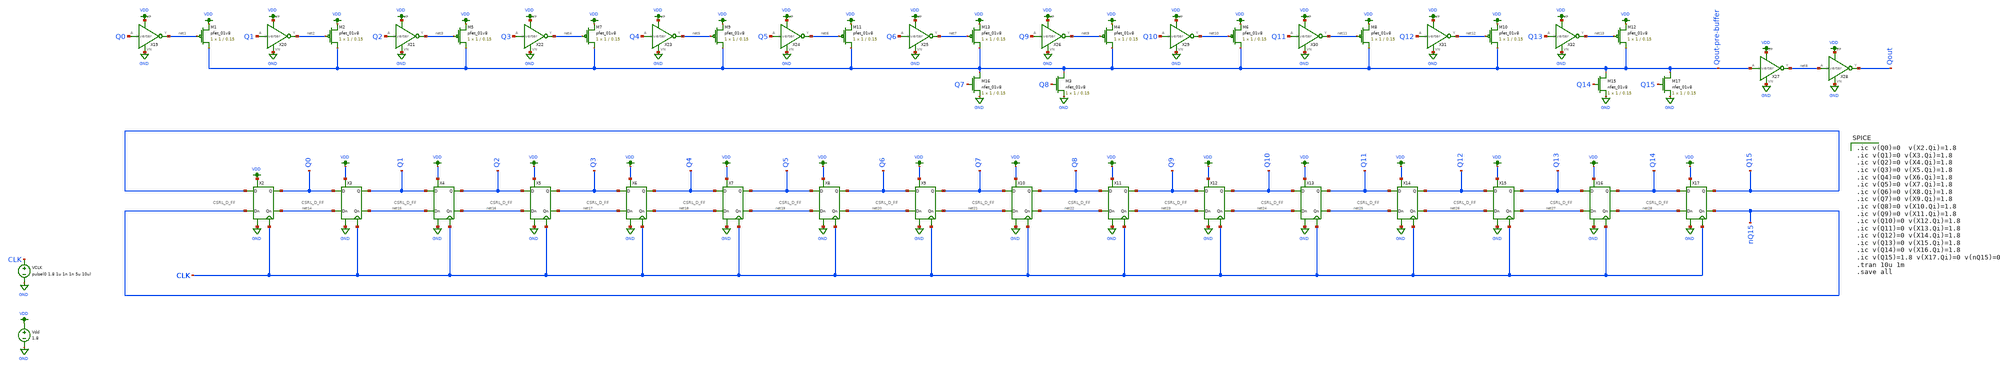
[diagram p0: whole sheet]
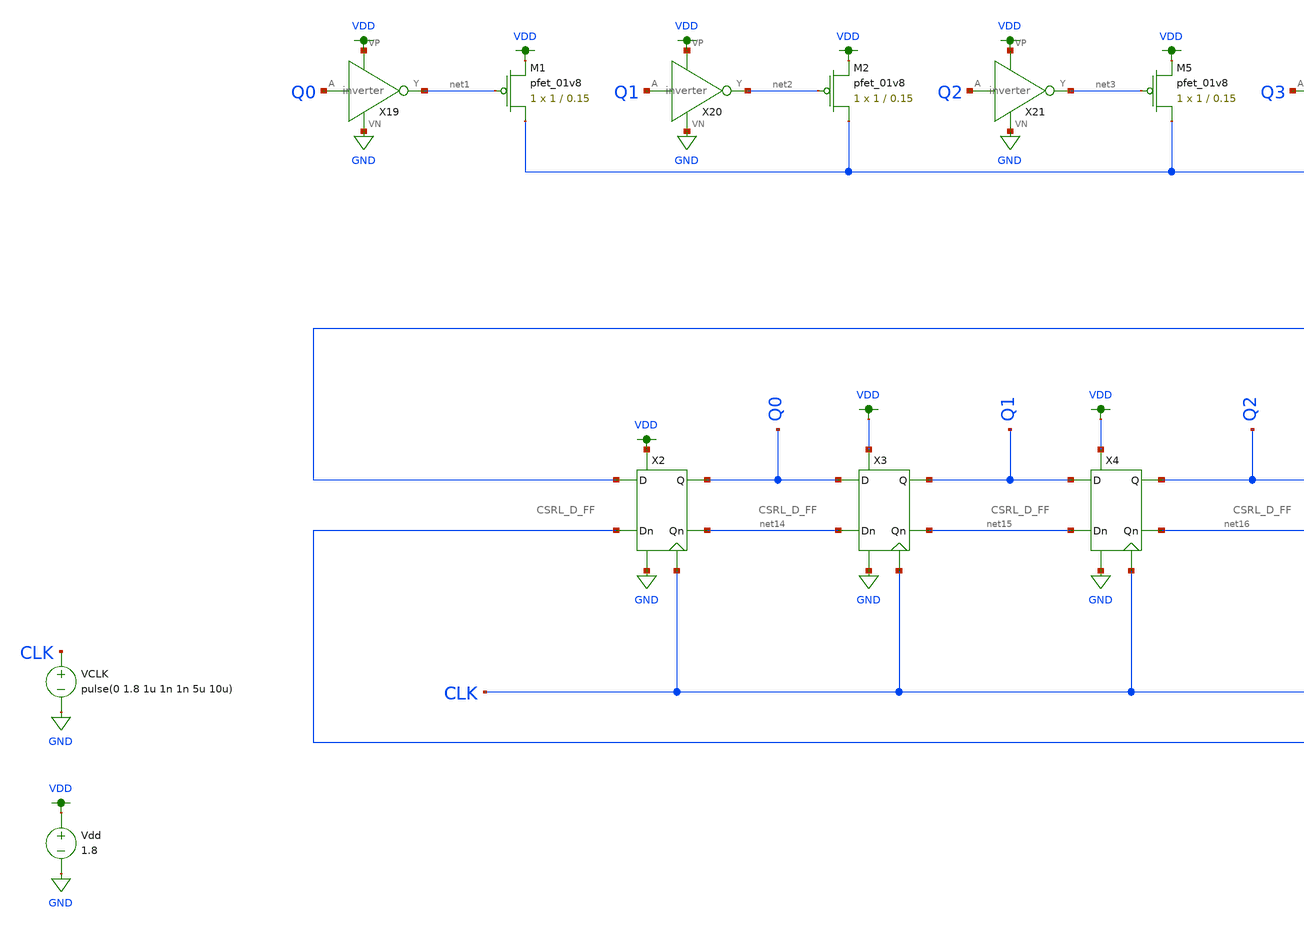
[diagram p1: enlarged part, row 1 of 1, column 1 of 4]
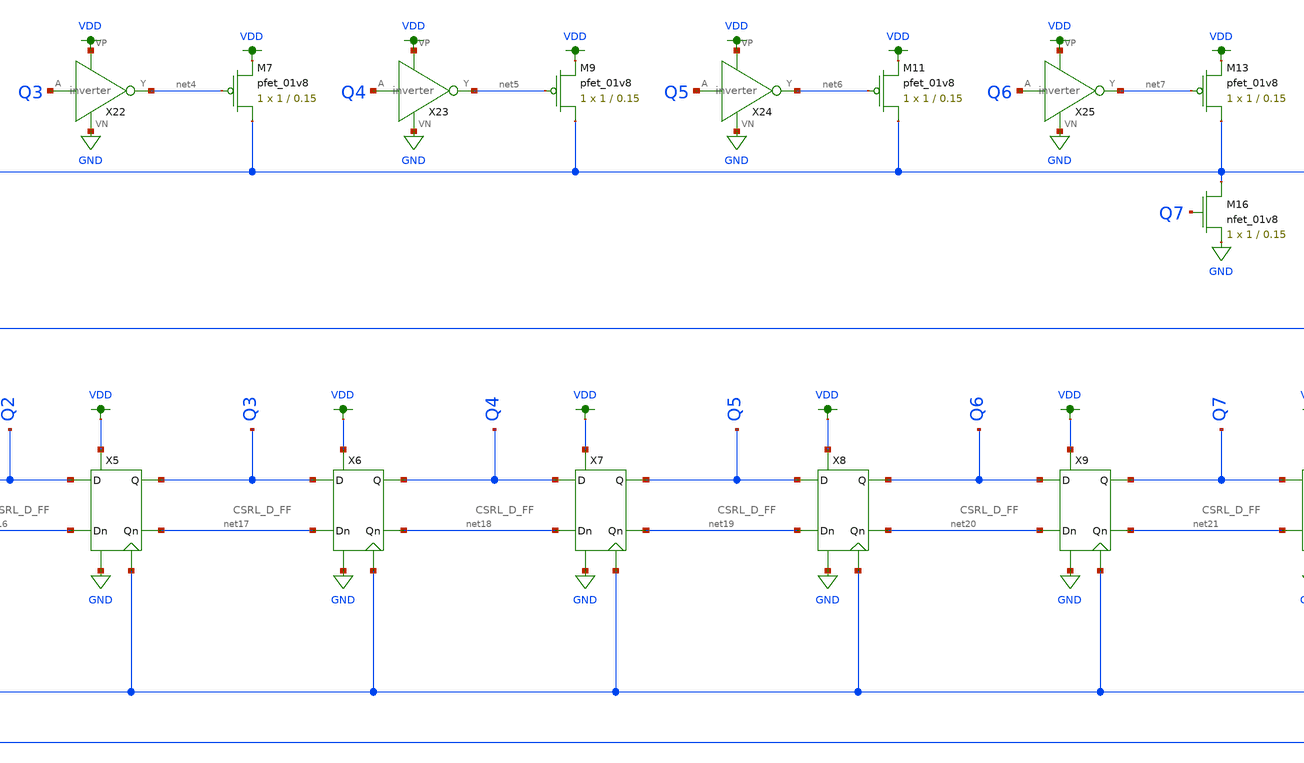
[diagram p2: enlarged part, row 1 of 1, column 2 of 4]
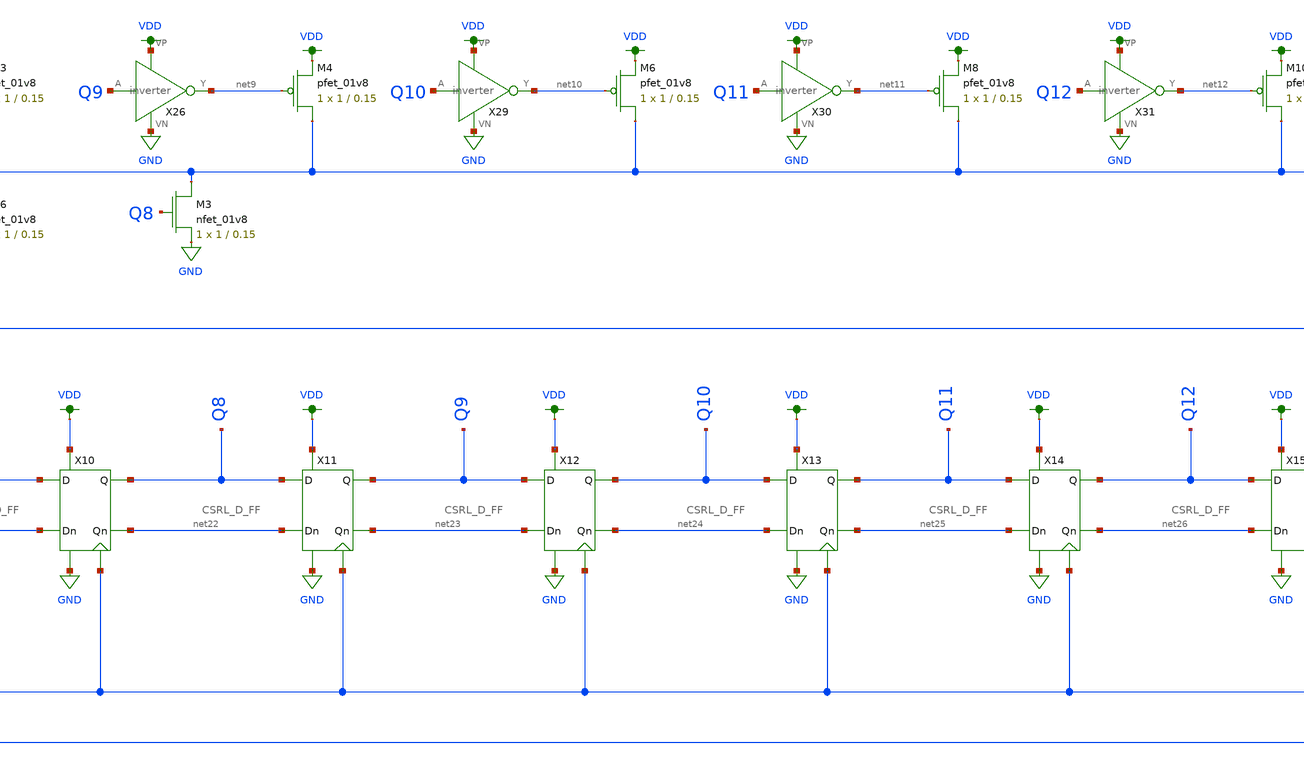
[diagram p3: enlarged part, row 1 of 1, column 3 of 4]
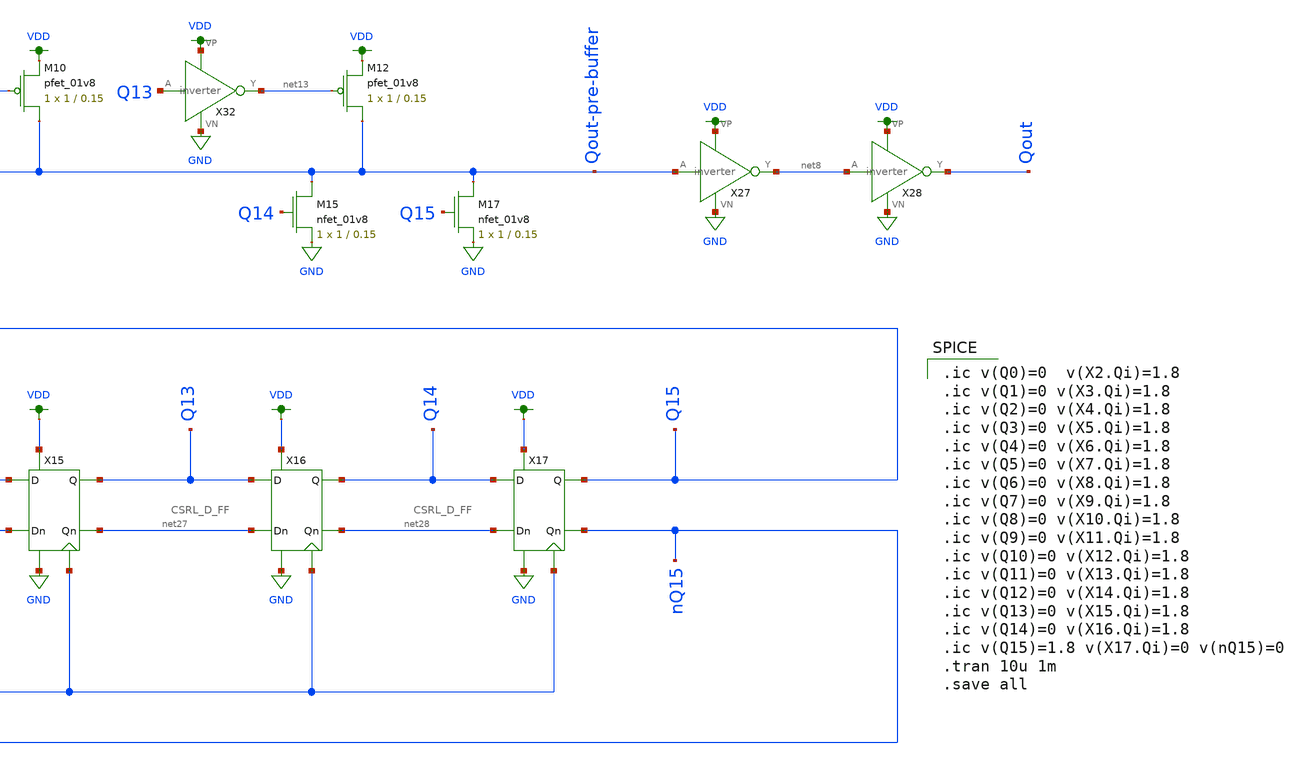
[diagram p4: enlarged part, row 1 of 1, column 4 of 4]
** sch_path: schematic/archive/phiF1.sch
**.subckt phiF1
VCLK CLK GND pulse(0 1.8 1u 1n 1n 5u 10u)
Vdd VDD GND 1.8
XM1 Qout-pre-buffer net1 VDD VDD sky130_fd_pr__pfet_01v8 L=0.15 W=1 nf=1 ad='int((nf+1)/2) * W/nf * 0.29'
+ as='int((nf+2)/2) * W/nf * 0.29' pd='2*int((nf+1)/2) * (W/nf + 0.29)' ps='2*int((nf+2)/2) * (W/nf + 0.29)'
+ nrd='0.29 / W' nrs='0.29 / W' sa=0 sb=0 sd=0 mult=1 m=1
XM2 Qout-pre-buffer net2 VDD VDD sky130_fd_pr__pfet_01v8 L=0.15 W=1 nf=1 ad='int((nf+1)/2) * W/nf * 0.29'
+ as='int((nf+2)/2) * W/nf * 0.29' pd='2*int((nf+1)/2) * (W/nf + 0.29)' ps='2*int((nf+2)/2) * (W/nf + 0.29)'
+ nrd='0.29 / W' nrs='0.29 / W' sa=0 sb=0 sd=0 mult=1 m=1
X19 Q0 net1 VDD GND inverter
X20 Q1 net2 VDD GND inverter
XM5 Qout-pre-buffer net3 VDD VDD sky130_fd_pr__pfet_01v8 L=0.15 W=1 nf=1 ad='int((nf+1)/2) * W/nf * 0.29'
+ as='int((nf+2)/2) * W/nf * 0.29' pd='2*int((nf+1)/2) * (W/nf + 0.29)' ps='2*int((nf+2)/2) * (W/nf + 0.29)'
+ nrd='0.29 / W' nrs='0.29 / W' sa=0 sb=0 sd=0 mult=1 m=1
X21 Q2 net3 VDD GND inverter
XM7 Qout-pre-buffer net4 VDD VDD sky130_fd_pr__pfet_01v8 L=0.15 W=1 nf=1 ad='int((nf+1)/2) * W/nf * 0.29'
+ as='int((nf+2)/2) * W/nf * 0.29' pd='2*int((nf+1)/2) * (W/nf + 0.29)' ps='2*int((nf+2)/2) * (W/nf + 0.29)'
+ nrd='0.29 / W' nrs='0.29 / W' sa=0 sb=0 sd=0 mult=1 m=1
X22 Q3 net4 VDD GND inverter
XM9 Qout-pre-buffer net5 VDD VDD sky130_fd_pr__pfet_01v8 L=0.15 W=1 nf=1 ad='int((nf+1)/2) * W/nf * 0.29'
+ as='int((nf+2)/2) * W/nf * 0.29' pd='2*int((nf+1)/2) * (W/nf + 0.29)' ps='2*int((nf+2)/2) * (W/nf + 0.29)'
+ nrd='0.29 / W' nrs='0.29 / W' sa=0 sb=0 sd=0 mult=1 m=1
X23 Q4 net5 VDD GND inverter
XM11 Qout-pre-buffer net6 VDD VDD sky130_fd_pr__pfet_01v8 L=0.15 W=1 nf=1 ad='int((nf+1)/2) * W/nf * 0.29'
+ as='int((nf+2)/2) * W/nf * 0.29' pd='2*int((nf+1)/2) * (W/nf + 0.29)' ps='2*int((nf+2)/2) * (W/nf + 0.29)'
+ nrd='0.29 / W' nrs='0.29 / W' sa=0 sb=0 sd=0 mult=1 m=1
X24 Q5 net6 VDD GND inverter
XM13 Qout-pre-buffer net7 VDD VDD sky130_fd_pr__pfet_01v8 L=0.15 W=1 nf=1 ad='int((nf+1)/2) * W/nf * 0.29'
+ as='int((nf+2)/2) * W/nf * 0.29' pd='2*int((nf+1)/2) * (W/nf + 0.29)' ps='2*int((nf+2)/2) * (W/nf + 0.29)'
+ nrd='0.29 / W' nrs='0.29 / W' sa=0 sb=0 sd=0 mult=1 m=1
X25 Q6 net7 VDD GND inverter
XM16 Qout-pre-buffer Q7 GND GND sky130_fd_pr__nfet_01v8 L=0.15 W=1 nf=1 ad='int((nf+1)/2) * W/nf * 0.29'
+ as='int((nf+2)/2) * W/nf * 0.29' pd='2*int((nf+1)/2) * (W/nf + 0.29)' ps='2*int((nf+2)/2) * (W/nf + 0.29)'
+ nrd='0.29 / W' nrs='0.29 / W' sa=0 sb=0 sd=0 mult=1 m=1
X27 Qout-pre-buffer net8 VDD GND inverter
X28 net8 Qout VDD GND inverter
XM3 Qout-pre-buffer Q8 GND GND sky130_fd_pr__nfet_01v8 L=0.15 W=1 nf=1 ad='int((nf+1)/2) * W/nf * 0.29'
+ as='int((nf+2)/2) * W/nf * 0.29' pd='2*int((nf+1)/2) * (W/nf + 0.29)' ps='2*int((nf+2)/2) * (W/nf + 0.29)'
+ nrd='0.29 / W' nrs='0.29 / W' sa=0 sb=0 sd=0 mult=1 m=1
XM4 Qout-pre-buffer net9 VDD VDD sky130_fd_pr__pfet_01v8 L=0.15 W=1 nf=1 ad='int((nf+1)/2) * W/nf * 0.29'
+ as='int((nf+2)/2) * W/nf * 0.29' pd='2*int((nf+1)/2) * (W/nf + 0.29)' ps='2*int((nf+2)/2) * (W/nf + 0.29)'
+ nrd='0.29 / W' nrs='0.29 / W' sa=0 sb=0 sd=0 mult=1 m=1
X26 Q9 net9 VDD GND inverter
XM6 Qout-pre-buffer net10 VDD VDD sky130_fd_pr__pfet_01v8 L=0.15 W=1 nf=1 ad='int((nf+1)/2) * W/nf * 0.29'
+ as='int((nf+2)/2) * W/nf * 0.29' pd='2*int((nf+1)/2) * (W/nf + 0.29)' ps='2*int((nf+2)/2) * (W/nf + 0.29)'
+ nrd='0.29 / W' nrs='0.29 / W' sa=0 sb=0 sd=0 mult=1 m=1
X29 Q10 net10 VDD GND inverter
XM8 Qout-pre-buffer net11 VDD VDD sky130_fd_pr__pfet_01v8 L=0.15 W=1 nf=1 ad='int((nf+1)/2) * W/nf * 0.29'
+ as='int((nf+2)/2) * W/nf * 0.29' pd='2*int((nf+1)/2) * (W/nf + 0.29)' ps='2*int((nf+2)/2) * (W/nf + 0.29)'
+ nrd='0.29 / W' nrs='0.29 / W' sa=0 sb=0 sd=0 mult=1 m=1
X30 Q11 net11 VDD GND inverter
XM10 Qout-pre-buffer net12 VDD VDD sky130_fd_pr__pfet_01v8 L=0.15 W=1 nf=1 ad='int((nf+1)/2) * W/nf * 0.29'
+ as='int((nf+2)/2) * W/nf * 0.29' pd='2*int((nf+1)/2) * (W/nf + 0.29)' ps='2*int((nf+2)/2) * (W/nf + 0.29)'
+ nrd='0.29 / W' nrs='0.29 / W' sa=0 sb=0 sd=0 mult=1 m=1
X31 Q12 net12 VDD GND inverter
XM12 Qout-pre-buffer net13 VDD VDD sky130_fd_pr__pfet_01v8 L=0.15 W=1 nf=1 ad='int((nf+1)/2) * W/nf * 0.29'
+ as='int((nf+2)/2) * W/nf * 0.29' pd='2*int((nf+1)/2) * (W/nf + 0.29)' ps='2*int((nf+2)/2) * (W/nf + 0.29)'
+ nrd='0.29 / W' nrs='0.29 / W' sa=0 sb=0 sd=0 mult=1 m=1
X32 Q13 net13 VDD GND inverter
XM15 Qout-pre-buffer Q14 GND GND sky130_fd_pr__nfet_01v8 L=0.15 W=1 nf=1 ad='int((nf+1)/2) * W/nf * 0.29'
+ as='int((nf+2)/2) * W/nf * 0.29' pd='2*int((nf+1)/2) * (W/nf + 0.29)' ps='2*int((nf+2)/2) * (W/nf + 0.29)'
+ nrd='0.29 / W' nrs='0.29 / W' sa=0 sb=0 sd=0 mult=1 m=1
XM17 Qout-pre-buffer Q15 GND GND sky130_fd_pr__nfet_01v8 L=0.15 W=1 nf=1 ad='int((nf+1)/2) * W/nf * 0.29'
+ as='int((nf+2)/2) * W/nf * 0.29' pd='2*int((nf+1)/2) * (W/nf + 0.29)' ps='2*int((nf+2)/2) * (W/nf + 0.29)'
+ nrd='0.29 / W' nrs='0.29 / W' sa=0 sb=0 sd=0 mult=1 m=1
X2 nQ15 Q15 net14 Q0 GND VDD CLK CSRL_D_FF
X3 net14 Q0 net15 Q1 GND VDD CLK CSRL_D_FF
X4 net15 Q1 net16 Q2 GND VDD CLK CSRL_D_FF
X5 net16 Q2 net17 Q3 GND VDD CLK CSRL_D_FF
X6 net17 Q3 net18 Q4 GND VDD CLK CSRL_D_FF
X7 net18 Q4 net19 Q5 GND VDD CLK CSRL_D_FF
X8 net19 Q5 net20 Q6 GND VDD CLK CSRL_D_FF
X9 net20 Q6 net21 Q7 GND VDD CLK CSRL_D_FF
X10 net21 Q7 net22 Q8 GND VDD CLK CSRL_D_FF
X11 net22 Q8 net23 Q9 GND VDD CLK CSRL_D_FF
X12 net23 Q9 net24 Q10 GND VDD CLK CSRL_D_FF
X13 net24 Q10 net25 Q11 GND VDD CLK CSRL_D_FF
X14 net25 Q11 net26 Q12 GND VDD CLK CSRL_D_FF
X15 net26 Q12 net27 Q13 GND VDD CLK CSRL_D_FF
X16 net27 Q13 net28 Q14 GND VDD CLK CSRL_D_FF
X17 net28 Q14 nQ15 Q15 GND VDD CLK CSRL_D_FF
**** begin user architecture code

.option wnflag=1
.param MC_SWITCH=0.0
.lib ~/skywater/skywater-pdk/libraries/sky130_fd_pr_ngspice/latest/models/sky130.lib.spice tt


.ic v(Q0)=0  v(X2.Qi)=1.8
.ic v(Q1)=0 v(X3.Qi)=1.8
.ic v(Q2)=0 v(X4.Qi)=1.8
.ic v(Q3)=0 v(X5.Qi)=1.8
.ic v(Q4)=0 v(X6.Qi)=1.8
.ic v(Q5)=0 v(X7.Qi)=1.8
.ic v(Q6)=0 v(X8.Qi)=1.8
.ic v(Q7)=0 v(X9.Qi)=1.8
.ic v(Q8)=0 v(X10.Qi)=1.8
.ic v(Q9)=0 v(X11.Qi)=1.8
.ic v(Q10)=0 v(X12.Qi)=1.8
.ic v(Q11)=0 v(X13.Qi)=1.8
.ic v(Q12)=0 v(X14.Qi)=1.8
.ic v(Q13)=0 v(X15.Qi)=1.8
.ic v(Q14)=0 v(X16.Qi)=1.8
.ic v(Q15)=1.8 v(X17.Qi)=0 v(nQ15)=0
.tran 10u 1m
.save all

**** end user architecture code
**.ends

* expanding   symbol:  /home/madvlsi/Documents/MADVLSI-Final_Project/schematic/inverter.sym # of
*+ pins=4
** sym_path: schematic/inverter.sym
** sch_path: schematic/inverter.sch
.subckt inverter A Y VP VN
*.opin Y
*.ipin A
*.iopin VP
*.iopin VN
XM3 Y A VP VDD sky130_fd_pr__pfet_01v8 L={Lp} W={Wp} nf=1 ad='int((nf+1)/2) * W/nf * 0.29' as='int((nf+2)/2) * W/nf * 0.29'
+ pd='2*int((nf+1)/2) * (W/nf + 0.29)' ps='2*int((nf+2)/2) * (W/nf + 0.29)' nrd='0.29 / W' nrs='0.29 / W'
+ sa=0 sb=0 sd=0 mult=1 m=1
XM4 Y A VP VDD sky130_fd_pr__pfet_01v8 L={Lp} W={Wp} nf=1 ad='int((nf+1)/2) * W/nf * 0.29' as='int((nf+2)/2) * W/nf * 0.29'
+ pd='2*int((nf+1)/2) * (W/nf + 0.29)' ps='2*int((nf+2)/2) * (W/nf + 0.29)' nrd='0.29 / W' nrs='0.29 / W'
+ sa=0 sb=0 sd=0 mult=1 m=1
XM5 Y A VN GND sky130_fd_pr__nfet_01v8 L={Lp} W={Wp} nf=1 ad='int((nf+1)/2) * W/nf * 0.29' as='int((nf+2)/2) * W/nf * 0.29'
+ pd='2*int((nf+1)/2) * (W/nf + 0.29)' ps='2*int((nf+2)/2) * (W/nf + 0.29)' nrd='0.29 / W' nrs='0.29 / W'
+ sa=0 sb=0 sd=0 mult=1 m=1
.ends


* expanding   symbol:  /home/madvlsi/Documents/MADVLSI-Final_Project/schematic/CSRL_D_FF.sym # of
*+ pins=7
** sym_path: schematic/CSRL_D_FF.sym
** sch_path: schematic/CSRL_D_FF.sch
.subckt CSRL_D_FF Dn D Qn Q VN VP CLK
*.ipin Dn
*.ipin D
*.iopin VP
*.iopin VN
*.iopin CLK
*.opin Qn
*.opin Q
XM1 net5 CLK VP VDD sky130_fd_pr__pfet_01v8 L=0.15 W=1 nf=1 ad='int((nf+1)/2) * W/nf * 0.29' as='int((nf+2)/2) * W/nf * 0.29'
+ pd='2*int((nf+1)/2) * (W/nf + 0.29)' ps='2*int((nf+2)/2) * (W/nf + 0.29)' nrd='0.29 / W' nrs='0.29 / W'
+ sa=0 sb=0 sd=0 mult=1 m=1
XM2 net6 CLK VP VDD sky130_fd_pr__pfet_01v8 L=0.15 W=1 nf=1 ad='int((nf+1)/2) * W/nf * 0.29' as='int((nf+2)/2) * W/nf * 0.29'
+ pd='2*int((nf+1)/2) * (W/nf + 0.29)' ps='2*int((nf+2)/2) * (W/nf + 0.29)' nrd='0.29 / W' nrs='0.29 / W'
+ sa=0 sb=0 sd=0 mult=1 m=1
XM3 net3 CLK Q GND sky130_fd_pr__nfet_01v8 L=0.15 W=1 nf=1 ad='int((nf+1)/2) * W/nf * 0.29' as='int((nf+2)/2) * W/nf * 0.29'
+ pd='2*int((nf+1)/2) * (W/nf + 0.29)' ps='2*int((nf+2)/2) * (W/nf + 0.29)' nrd='0.29 / W' nrs='0.29 / W'
+ sa=0 sb=0 sd=0 mult=1 m=1
XM4 net4 CLK Qn GND sky130_fd_pr__nfet_01v8 L=0.15 W=1 nf=1 ad='int((nf+1)/2) * W/nf * 0.29' as='int((nf+2)/2) * W/nf * 0.29'
+ pd='2*int((nf+1)/2) * (W/nf + 0.29)' ps='2*int((nf+2)/2) * (W/nf + 0.29)' nrd='0.29 / W' nrs='0.29 / W'
+ sa=0 sb=0 sd=0 mult=1 m=1
XM5 Q Qn net6 VDD sky130_fd_pr__pfet_01v8 L=0.15 W=1 nf=1 ad='int((nf+1)/2) * W/nf * 0.29' as='int((nf+2)/2) * W/nf * 0.29'
+ pd='2*int((nf+1)/2) * (W/nf + 0.29)' ps='2*int((nf+2)/2) * (W/nf + 0.29)' nrd='0.29 / W' nrs='0.29 / W'
+ sa=0 sb=0 sd=0 mult=1 m=1
XM6 VN Qn Q GND sky130_fd_pr__nfet_01v8 L=0.15 W=1 nf=1 ad='int((nf+1)/2) * W/nf * 0.29' as='int((nf+2)/2) * W/nf * 0.29'
+ pd='2*int((nf+1)/2) * (W/nf + 0.29)' ps='2*int((nf+2)/2) * (W/nf + 0.29)' nrd='0.29 / W' nrs='0.29 / W'
+ sa=0 sb=0 sd=0 mult=1 m=1
XM7 Qn Q net5 VDD sky130_fd_pr__pfet_01v8 L=0.15 W=1 nf=1 ad='int((nf+1)/2) * W/nf * 0.29' as='int((nf+2)/2) * W/nf * 0.29'
+ pd='2*int((nf+1)/2) * (W/nf + 0.29)' ps='2*int((nf+2)/2) * (W/nf + 0.29)' nrd='0.29 / W' nrs='0.29 / W'
+ sa=0 sb=0 sd=0 mult=1 m=1
XM8 VN Q Qn GND sky130_fd_pr__nfet_01v8 L=0.15 W=1 nf=1 ad='int((nf+1)/2) * W/nf * 0.29' as='int((nf+2)/2) * W/nf * 0.29'
+ pd='2*int((nf+1)/2) * (W/nf + 0.29)' ps='2*int((nf+2)/2) * (W/nf + 0.29)' nrd='0.29 / W' nrs='0.29 / W'
+ sa=0 sb=0 sd=0 mult=1 m=1
XM9 net4 CLK Dn VDD sky130_fd_pr__pfet_01v8 L=0.15 W=1 nf=1 ad='int((nf+1)/2) * W/nf * 0.29' as='int((nf+2)/2) * W/nf * 0.29'
+ pd='2*int((nf+1)/2) * (W/nf + 0.29)' ps='2*int((nf+2)/2) * (W/nf + 0.29)' nrd='0.29 / W' nrs='0.29 / W'
+ sa=0 sb=0 sd=0 mult=1 m=1
XM10 net3 CLK D VDD sky130_fd_pr__pfet_01v8 L=0.15 W=1 nf=1 ad='int((nf+1)/2) * W/nf * 0.29' as='int((nf+2)/2) * W/nf * 0.29'
+ pd='2*int((nf+1)/2) * (W/nf + 0.29)' ps='2*int((nf+2)/2) * (W/nf + 0.29)' nrd='0.29 / W' nrs='0.29 / W'
+ sa=0 sb=0 sd=0 mult=1 m=1
XM11 VN CLK net1 GND sky130_fd_pr__nfet_01v8 L=0.15 W=1 nf=1 ad='int((nf+1)/2) * W/nf * 0.29' as='int((nf+2)/2) * W/nf * 0.29'
+ pd='2*int((nf+1)/2) * (W/nf + 0.29)' ps='2*int((nf+2)/2) * (W/nf + 0.29)' nrd='0.29 / W' nrs='0.29 / W'
+ sa=0 sb=0 sd=0 mult=1 m=1
XM12 VN CLK net2 GND sky130_fd_pr__nfet_01v8 L=0.15 W=1 nf=1 ad='int((nf+1)/2) * W/nf * 0.29' as='int((nf+2)/2) * W/nf * 0.29'
+ pd='2*int((nf+1)/2) * (W/nf + 0.29)' ps='2*int((nf+2)/2) * (W/nf + 0.29)' nrd='0.29 / W' nrs='0.29 / W'
+ sa=0 sb=0 sd=0 mult=1 m=1
XM13 VP net3 net4 VDD sky130_fd_pr__pfet_01v8 L=0.15 W=1 nf=1 ad='int((nf+1)/2) * W/nf * 0.29' as='int((nf+2)/2) * W/nf * 0.29'
+ pd='2*int((nf+1)/2) * (W/nf + 0.29)' ps='2*int((nf+2)/2) * (W/nf + 0.29)' nrd='0.29 / W' nrs='0.29 / W'
+ sa=0 sb=0 sd=0 mult=1 m=1
XM14 VP net4 net3 VDD sky130_fd_pr__pfet_01v8 L=0.15 W=1 nf=1 ad='int((nf+1)/2) * W/nf * 0.29' as='int((nf+2)/2) * W/nf * 0.29'
+ pd='2*int((nf+1)/2) * (W/nf + 0.29)' ps='2*int((nf+2)/2) * (W/nf + 0.29)' nrd='0.29 / W' nrs='0.29 / W'
+ sa=0 sb=0 sd=0 mult=1 m=1
XM15 net3 net4 net1 GND sky130_fd_pr__nfet_01v8 L=0.15 W=1 nf=1 ad='int((nf+1)/2) * W/nf * 0.29' as='int((nf+2)/2) * W/nf * 0.29'
+ pd='2*int((nf+1)/2) * (W/nf + 0.29)' ps='2*int((nf+2)/2) * (W/nf + 0.29)' nrd='0.29 / W' nrs='0.29 / W'
+ sa=0 sb=0 sd=0 mult=1 m=1
XM16 net4 net3 net2 GND sky130_fd_pr__nfet_01v8 L=0.15 W=1 nf=1 ad='int((nf+1)/2) * W/nf * 0.29' as='int((nf+2)/2) * W/nf * 0.29'
+ pd='2*int((nf+1)/2) * (W/nf + 0.29)' ps='2*int((nf+2)/2) * (W/nf + 0.29)' nrd='0.29 / W' nrs='0.29 / W'
+ sa=0 sb=0 sd=0 mult=1 m=1
XM17 VN CLK net2 GND sky130_fd_pr__nfet_01v8 L=0.15 W=1 nf=1 ad='int((nf+1)/2) * W/nf * 0.29' as='int((nf+2)/2) * W/nf * 0.29'
+ pd='2*int((nf+1)/2) * (W/nf + 0.29)' ps='2*int((nf+2)/2) * (W/nf + 0.29)' nrd='0.29 / W' nrs='0.29 / W'
+ sa=0 sb=0 sd=0 mult=1 m=1
XM18 VN CLK net1 GND sky130_fd_pr__nfet_01v8 L=0.15 W=1 nf=1 ad='int((nf+1)/2) * W/nf * 0.29' as='int((nf+2)/2) * W/nf * 0.29'
+ pd='2*int((nf+1)/2) * (W/nf + 0.29)' ps='2*int((nf+2)/2) * (W/nf + 0.29)' nrd='0.29 / W' nrs='0.29 / W'
+ sa=0 sb=0 sd=0 mult=1 m=1
.ends

.GLOBAL GND
.GLOBAL VDD
.end
